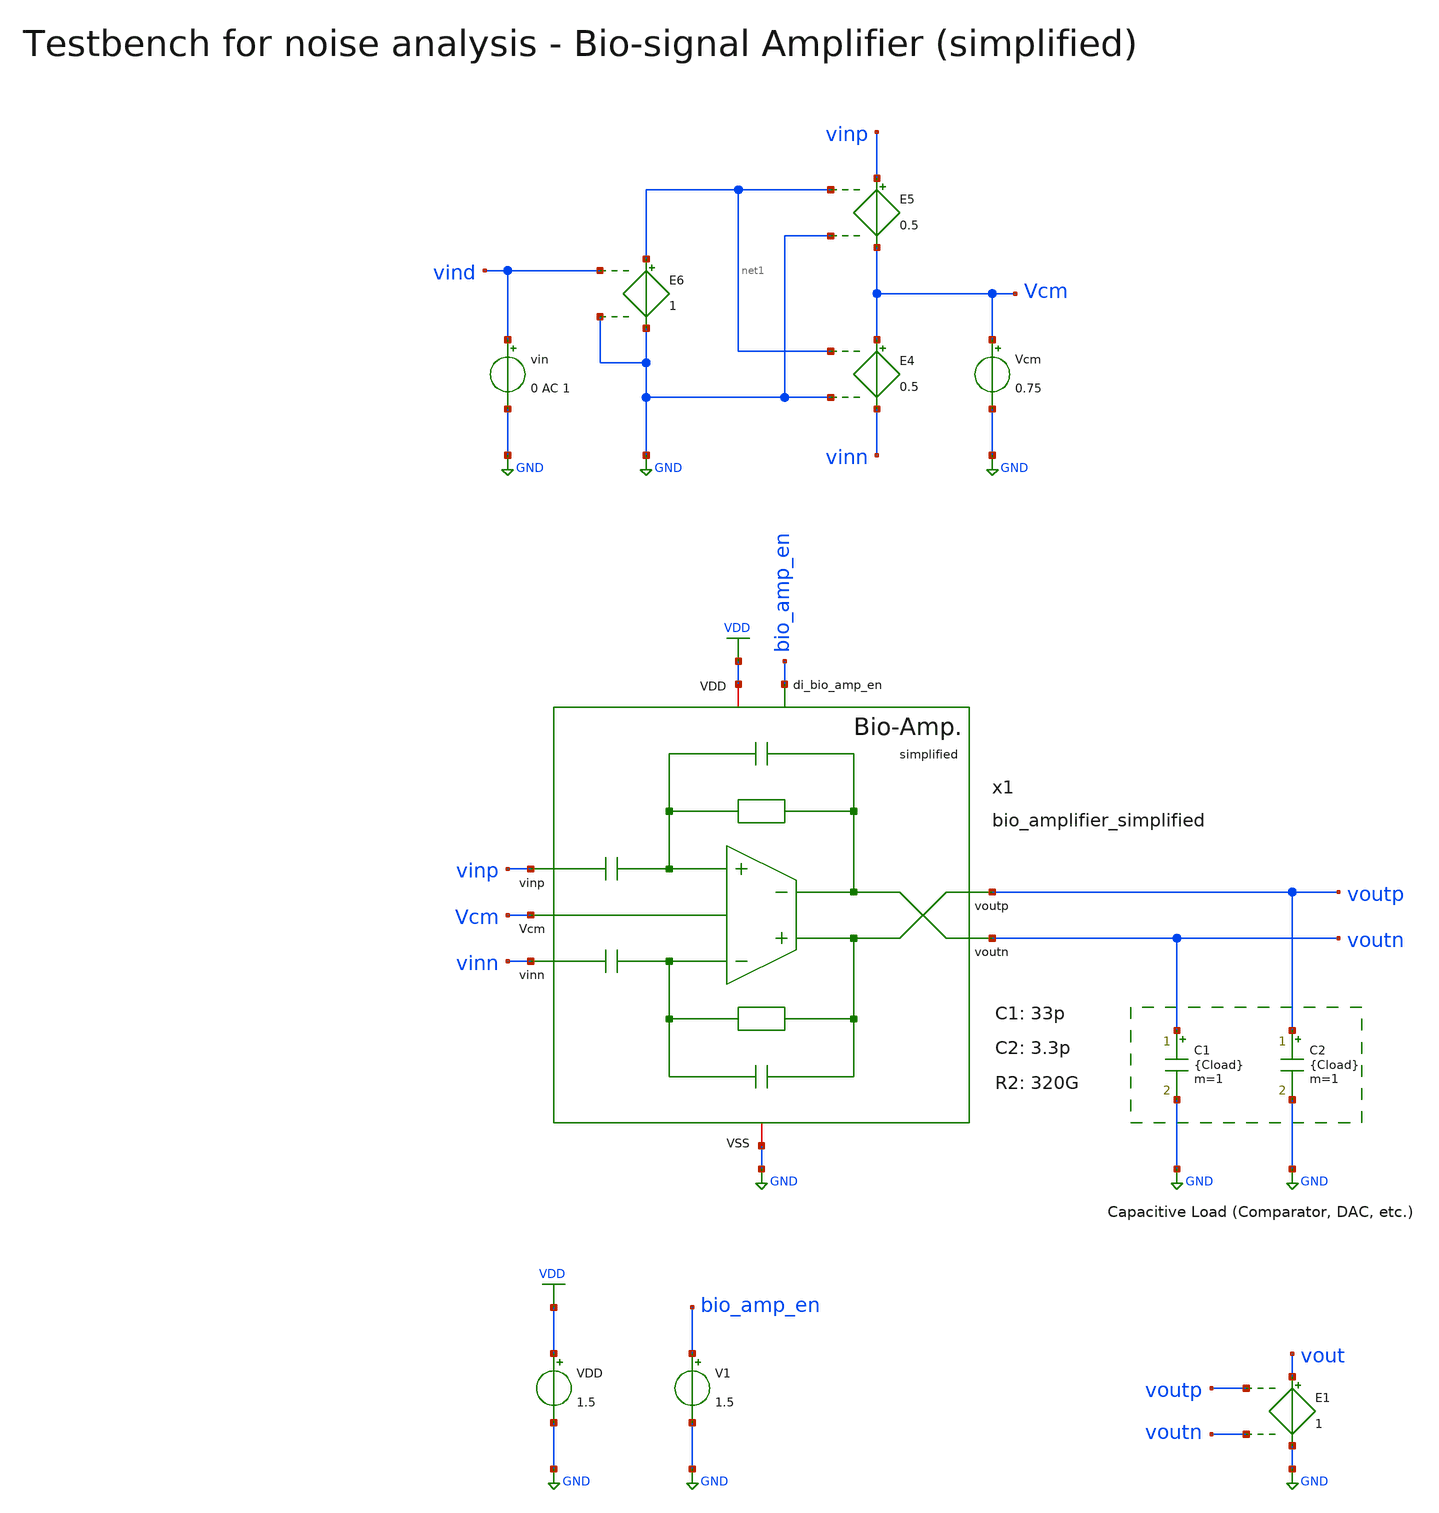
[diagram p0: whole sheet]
** sch_path: SG13G2_ATBS-ADC-main/xschem/bio_amplifier/testbenches/bio_amplifier_simplified_tb_noise.sch
**.subckt bio_amplifier_simplified_tb_noise
VDD VDD GND 1.5
C1 voutn GND {Cload} m=1
C2 voutp GND {Cload} m=1
Vcm Vcm GND 0.75
E4 Vcm vinn net1 GND 0.5
E5 vinp Vcm net1 GND 0.5
E6 net1 GND vind GND 1
V1 bio_amp_en GND 1.5
E1 vout GND voutp voutn 1
vin vind GND 0 AC 1
x1 voutp bio_amp_en vinp Vcm voutn vinn VDD GND bio_amplifier_simplified C1=33p C2=3.3p R2=320G
**** begin user architecture code

.lib cornerMOSlv.lib mos_tt
.lib cornerMOShv.lib mos_tt
.lib cornerRES.lib res_typ



.param temp=27
* 227.56fF DAC
.param Cload=227.56f
.options savecurrents method=gear reltol=1e-2 abstol=1e-12 gmin=1e-15
.control

optran 0 0 0 1u 1m 0

save all

set enable_noisy_r

* User Constants
let f_min = 0.15
let f_max = 500
* let f_min = 100u
* let f_max = 1k

* Operating Point Analysis
op
remzerovec
write bio_amplifier_simplified_tb_noise.raw
set appendwrite

* Noise Analysis
noise v(vout) vin dec 101 $&const.f_min $&const.f_max 1

* Plotting
setplot noise1
plot inoise_spectrum ylog xlog ylabel 'Input Noise'
plot onoise_spectrum ylog xlog ylabel 'Output Noise'
write bio_amplifier_simplified_tb_noise.raw

* Write Data
set wr_vecnames
set wr_singlescale
wrdata
+ /foss/designs/SG13G2_ATBS-ADC-main/python/plot_simulations/data/bio_amplifier_simplified_tb_noise.txt v(inoise_spectrum) v(onoise_spectrum)

* Measurements
setplot noise2
print inoise_total
print onoise_total

*quit
.endc


**** end user architecture code
**.ends
.GLOBAL GND
.GLOBAL VDD
.end
